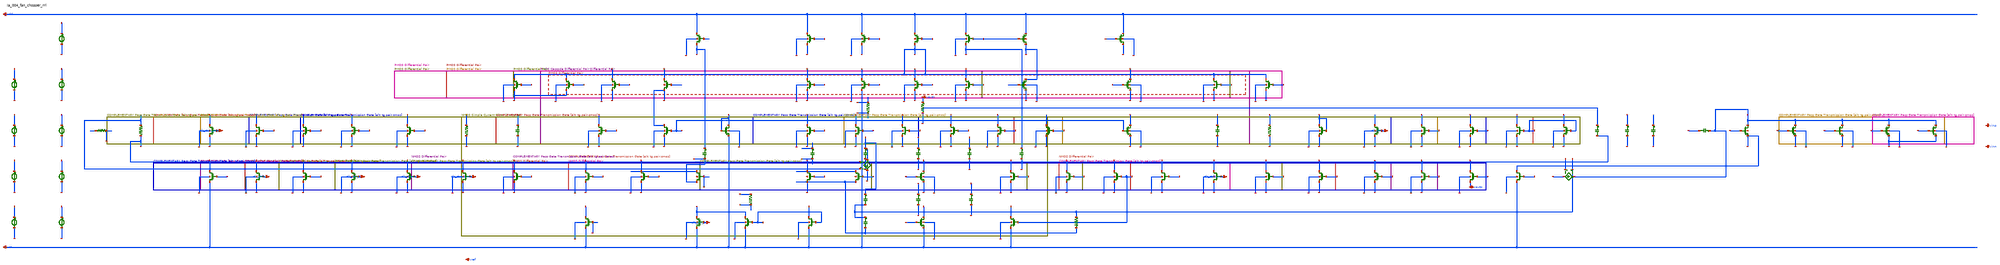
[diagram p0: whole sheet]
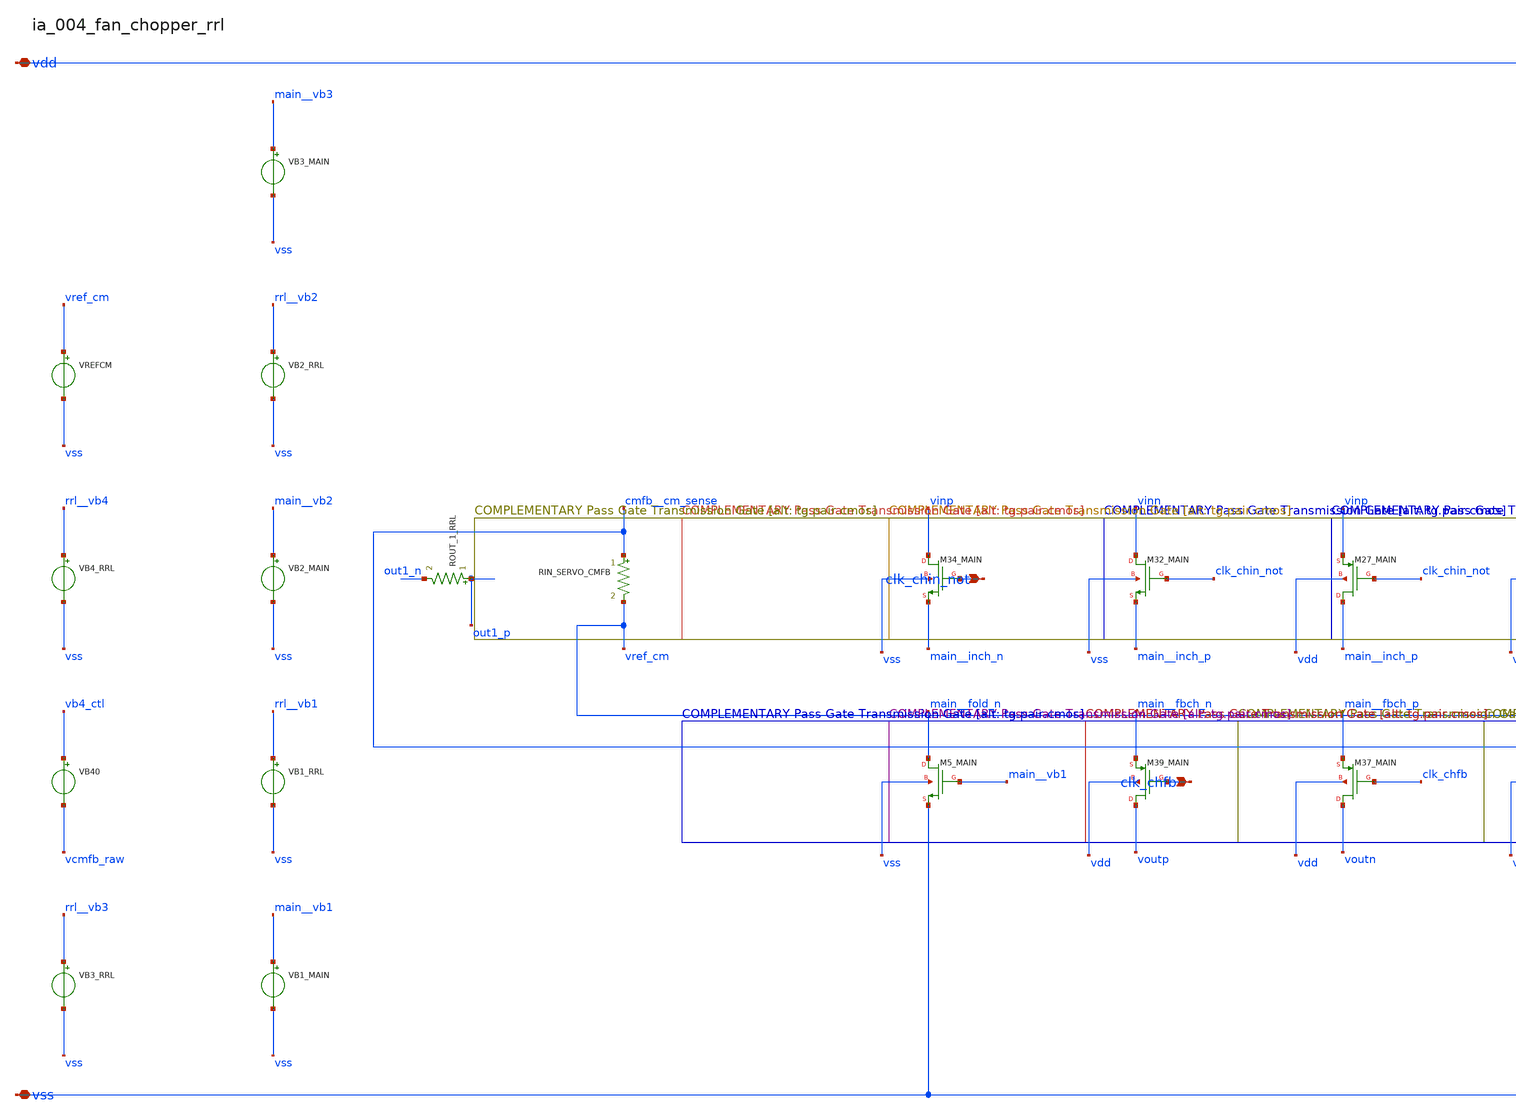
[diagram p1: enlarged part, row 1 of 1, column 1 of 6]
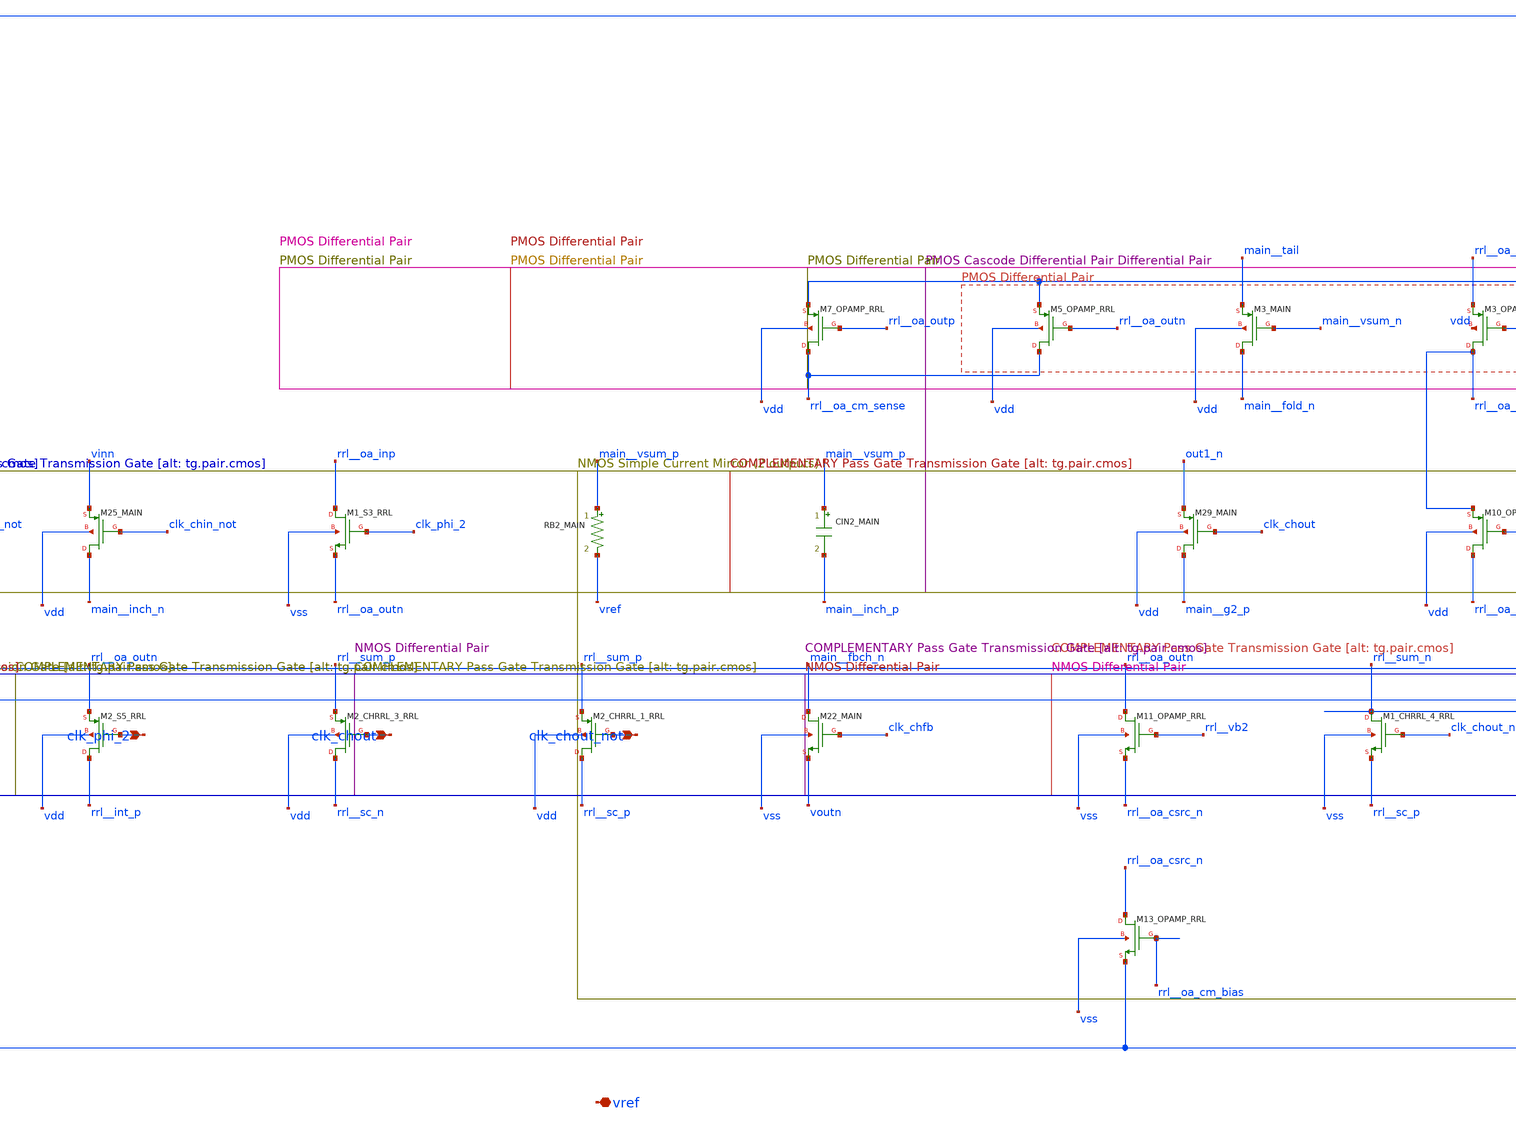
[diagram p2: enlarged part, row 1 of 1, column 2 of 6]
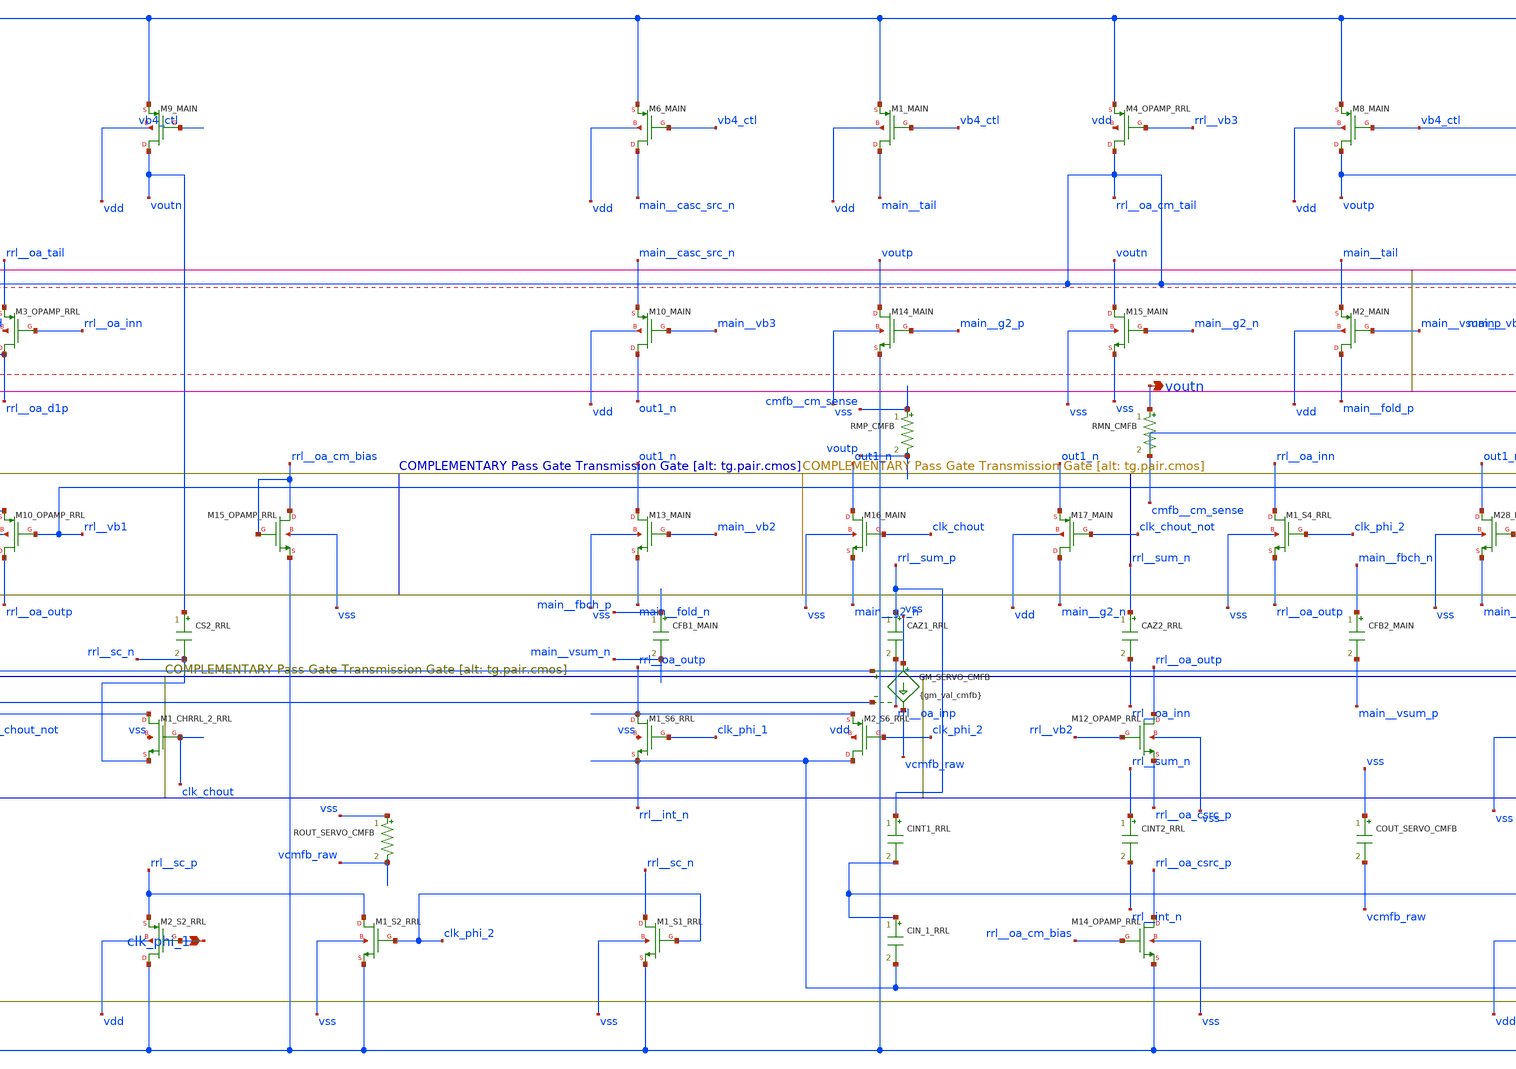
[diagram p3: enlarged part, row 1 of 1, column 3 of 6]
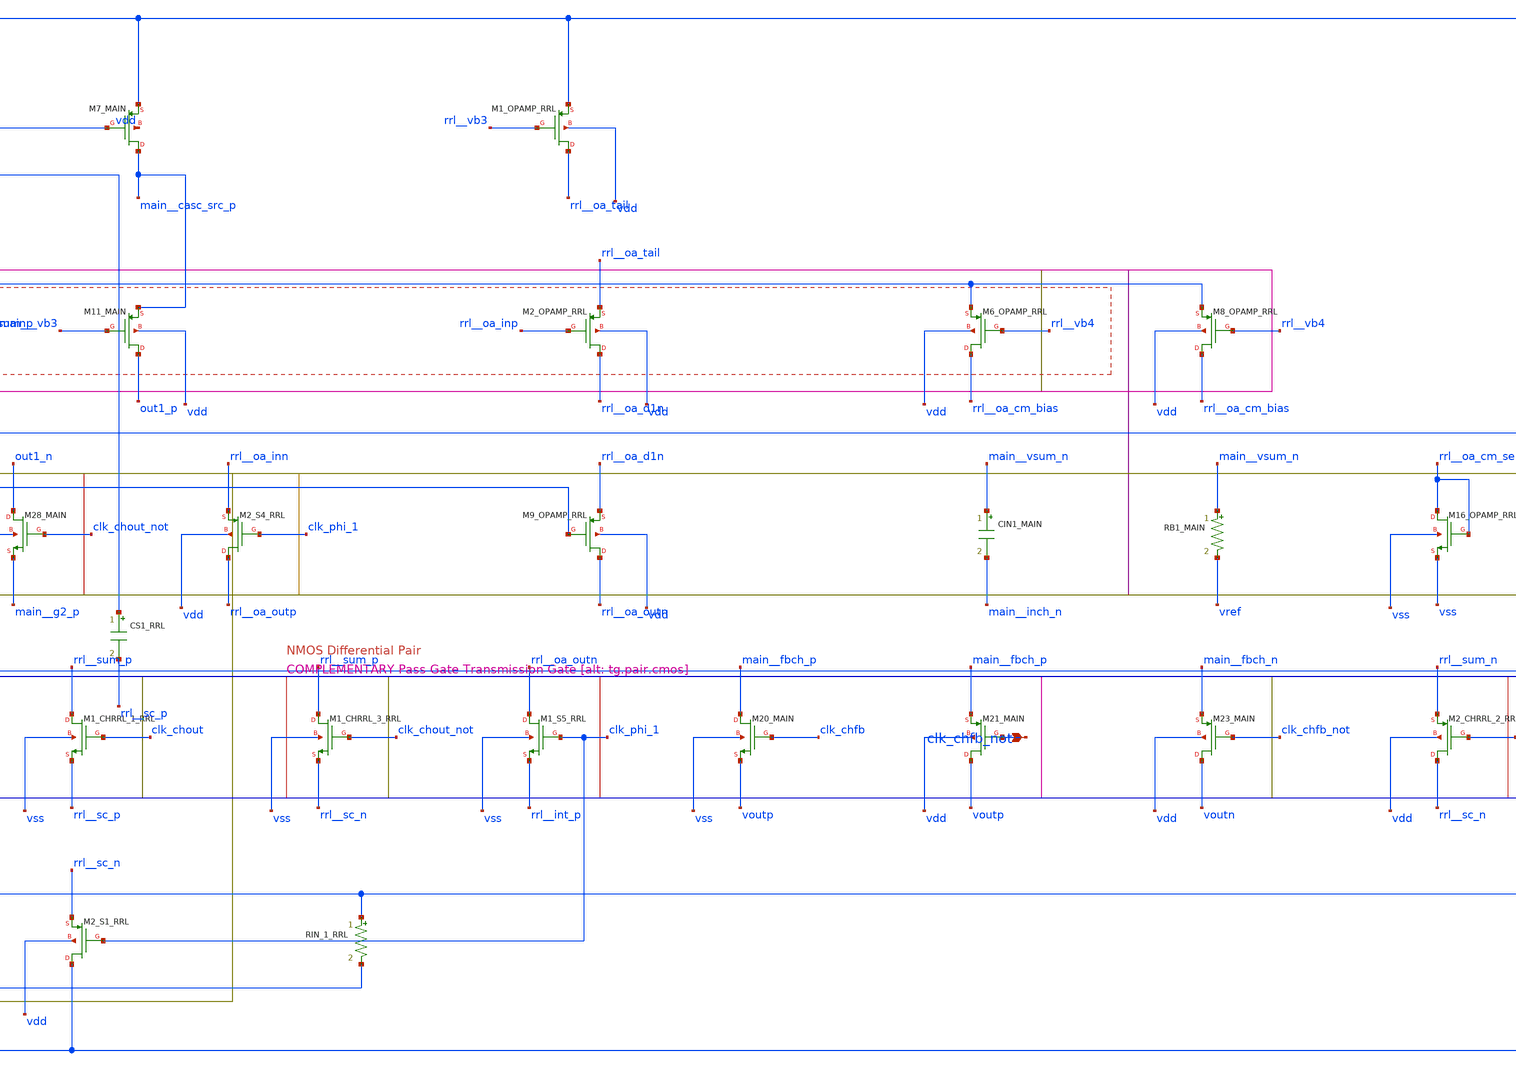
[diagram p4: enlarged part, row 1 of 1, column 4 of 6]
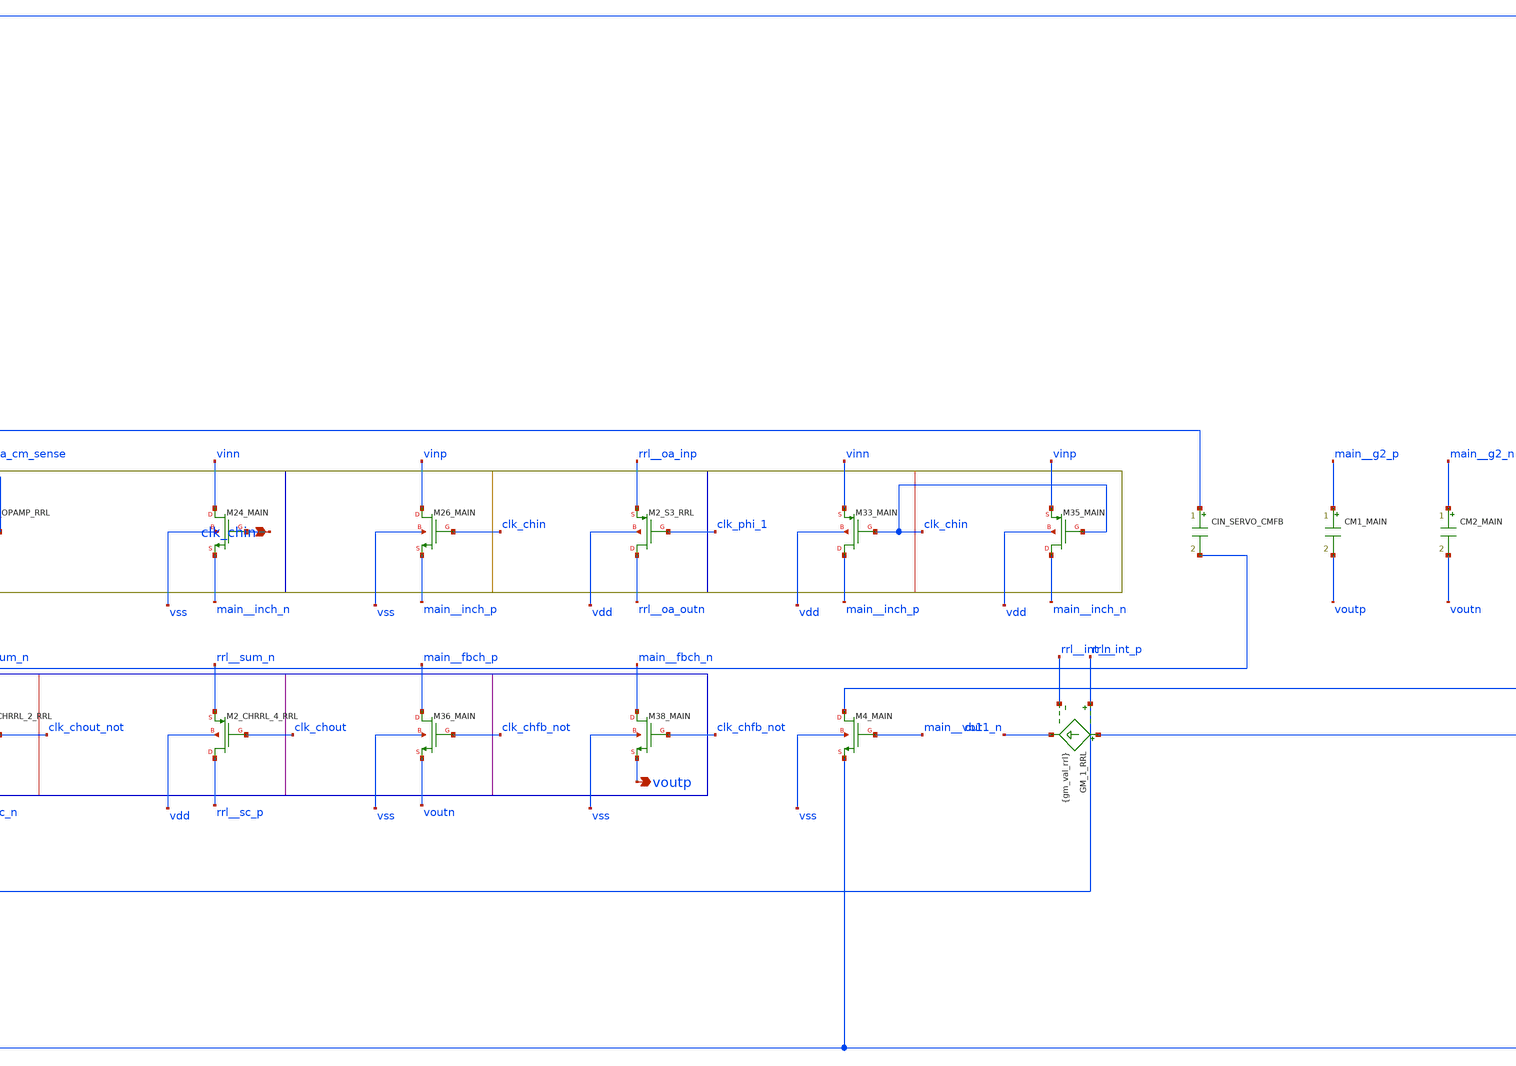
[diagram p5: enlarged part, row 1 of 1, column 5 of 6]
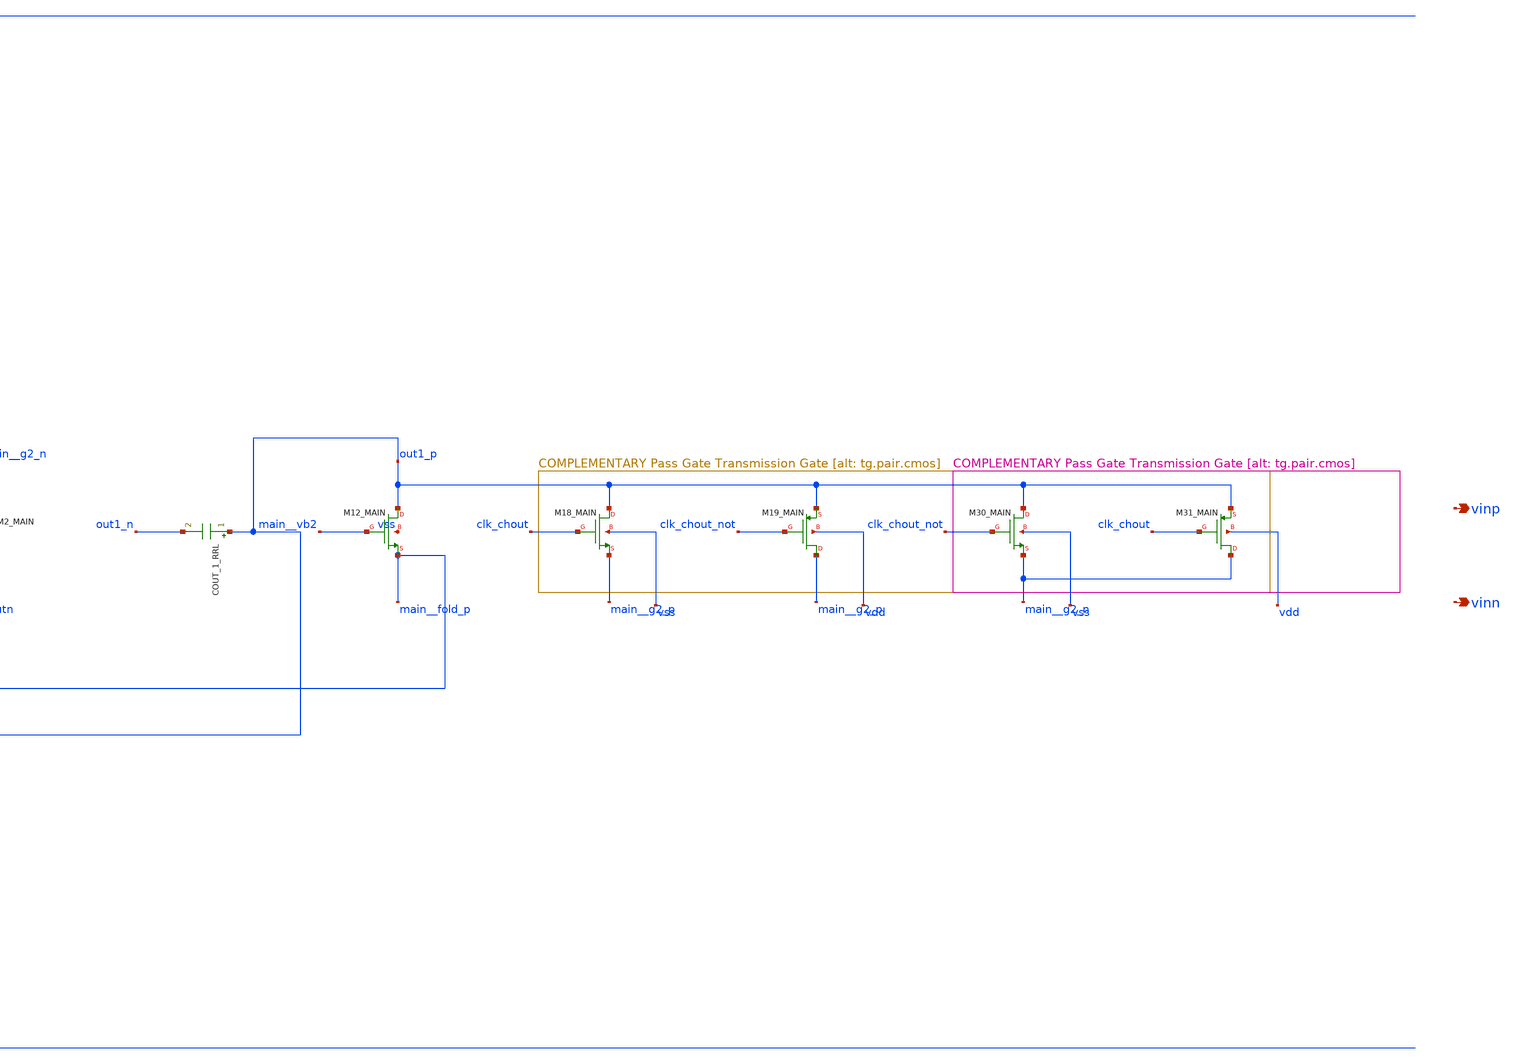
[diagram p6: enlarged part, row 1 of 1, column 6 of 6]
** sch_path: analog-db/raw/ia_004_fan_chopper_rrl/ia_004_fan_chopper_rrl_annotated.sch
**.subckt ia_004_fan_chopper_rrl_annotated clk_chin_not clk_phi_2 clk_chout clk_chout_not clk_phi_1
*+ clk_chin clk_chfb clk_chfb_not vdd vss voutn voutp vref vinp vinn
*.ipin clk_chin_not
*.ipin clk_phi_2
*.ipin clk_chout
*.ipin clk_chout_not
*.ipin clk_phi_1
*.ipin clk_chin
*.ipin clk_chfb
*.ipin clk_chfb_not
*.iopin vdd
*.iopin vss
*.opin voutn
*.opin voutp
*.iopin vref
*.opin vinp
*.opin vinn
CAZ1_RRL rrl__sum_p rrl__oa_inp 'x_dut_caz1_rrl_value' m=1
CAZ2_RRL rrl__sum_n rrl__oa_inn 'x_dut_caz2_rrl_value' m=1
CFB1_MAIN main__fbch_p main__vsum_n 'x_dut_cfb1_main_value' m=1
CFB2_MAIN main__fbch_n main__vsum_p 'x_dut_cfb2_main_value' m=1
CIN1_MAIN main__vsum_n main__inch_n 'x_dut_cin1_main_value' m=1
CIN2_MAIN main__vsum_p main__inch_p 'x_dut_cin2_main_value' m=1
CINT1_RRL rrl__sum_p rrl__int_p 'x_dut_cint1_rrl_value' m=1
CINT2_RRL rrl__sum_n rrl__int_n 'x_dut_cint2_rrl_value' m=1
CIN_1_RRL rrl__int_p rrl__int_n 'cin_val_rrl' m=1
CIN_SERVO_CMFB cmfb__cm_sense vref_cm 'cin_val_cmfb' m=1
CM1_MAIN main__g2_p voutp 'x_dut_cm1_main_value' m=1
CM2_MAIN main__g2_n voutn 'x_dut_cm2_main_value' m=1
COUT_1_RRL out1_p out1_n 'cout_val_rrl' m=1
COUT_SERVO_CMFB vss vcmfb_raw 'cout_val_cmfb' m=1
CS1_RRL voutp rrl__sc_p 'x_dut_cs1_rrl_value' m=1
CS2_RRL voutn rrl__sc_n 'x_dut_cs2_rrl_value' m=1
GM_1_RRL out1_p out1_n rrl__int_p rrl__int_n {gm_val_rrl}
GM_SERVO_CMFB vss vcmfb_raw vref_cm cmfb__cm_sense {gm_val_cmfb}
RB1_MAIN main__vsum_n vref 'x_dut_rb1_main_value' m=1
RB2_MAIN main__vsum_p vref 'x_dut_rb2_main_value' m=1
RIN_1_RRL rrl__int_p rrl__int_n 'rin_val_rrl' m=1
RIN_SERVO_CMFB cmfb__cm_sense vref_cm 'rin_val_cmfb' m=1
RMN_CMFB voutn cmfb__cm_sense 'x_dut_rmn_cmfb_value' m=1
RMP_CMFB cmfb__cm_sense voutp 'x_dut_rmp_cmfb_value' m=1
ROUT_1_RRL out1_p out1_n 'rout_val_rrl' m=1
ROUT_SERVO_CMFB vss vcmfb_raw 'rout_val_cmfb' m=1
VB1_MAIN main__vb1 vss dc {vb1_main}
VB1_RRL rrl__vb1 vss dc {vb1_rrl}
VB2_MAIN main__vb2 vss dc {vb2_main}
VB2_RRL rrl__vb2 vss dc {vb2_rrl}
VB3_MAIN main__vb3 vss dc {vb3_main}
VB3_RRL rrl__vb3 vss dc {vb3_rrl}
VB40 vb4_ctl vcmfb_raw dc {vb40}
VB4_RRL rrl__vb4 vss dc {vb4_rrl}
VREFCM vref_cm vss dc {vcm_ref}
XM10_MAIN out1_n main__vb3 main__casc_src_n vdd sg13_lv_pmos w=x_dut_xm10_main_w l=x_dut_xm10_main_l
+ ng=1 m=x_dut_xm10_main_m
XM10_OPAMP_RRL rrl__oa_outp rrl__vb1 rrl__oa_d1p vdd sg13_lv_pmos w=x_dut_xm10_opamp_rrl_w
+ l=x_dut_xm10_opamp_rrl_l ng=1 m=x_dut_xm10_opamp_rrl_m
XM11_MAIN out1_p main__vb3 main__casc_src_p vdd sg13_lv_pmos w=x_dut_xm11_main_w l=x_dut_xm11_main_l
+ ng=1 m=x_dut_xm11_main_m
XM11_OPAMP_RRL rrl__oa_outn rrl__vb2 rrl__oa_csrc_n vss sg13_lv_nmos w=x_dut_xm11_opamp_rrl_w
+ l=x_dut_xm11_opamp_rrl_l ng=1 m=x_dut_xm11_opamp_rrl_m
XM12_MAIN out1_p main__vb2 main__fold_p vss sg13_lv_nmos w=x_dut_xm12_main_w l=x_dut_xm12_main_l
+ ng=1 m=x_dut_xm12_main_m
XM12_OPAMP_RRL rrl__oa_outp rrl__vb2 rrl__oa_csrc_p vss sg13_lv_nmos w=x_dut_xm12_opamp_rrl_w
+ l=x_dut_xm12_opamp_rrl_l ng=1 m=x_dut_xm12_opamp_rrl_m
XM13_MAIN out1_n main__vb2 main__fold_n vss sg13_lv_nmos w=x_dut_xm13_main_w l=x_dut_xm13_main_l
+ ng=1 m=x_dut_xm13_main_m
XM13_OPAMP_RRL rrl__oa_csrc_n rrl__oa_cm_bias vss vss sg13_lv_nmos w=x_dut_xm13_opamp_rrl_w
+ l=x_dut_xm13_opamp_rrl_l ng=1 m=x_dut_xm13_opamp_rrl_m
XM14_MAIN voutp main__g2_p vss vss sg13_lv_nmos w=x_dut_xm14_main_w l=x_dut_xm14_main_l ng=1
+ m=x_dut_xm14_main_m
XM14_OPAMP_RRL rrl__oa_csrc_p rrl__oa_cm_bias vss vss sg13_lv_nmos w=x_dut_xm14_opamp_rrl_w
+ l=x_dut_xm14_opamp_rrl_l ng=1 m=x_dut_xm14_opamp_rrl_m
XM15_MAIN voutn main__g2_n vss vss sg13_lv_nmos w=x_dut_xm15_main_w l=x_dut_xm15_main_l ng=1
+ m=x_dut_xm15_main_m
XM15_OPAMP_RRL rrl__oa_cm_bias rrl__oa_cm_bias vss vss sg13_lv_nmos w=x_dut_xm15_opamp_rrl_w
+ l=x_dut_xm15_opamp_rrl_l ng=1 m=x_dut_xm15_opamp_rrl_m
XM16_MAIN out1_n clk_chout main__g2_n vss sg13_lv_nmos w=x_dut_xm16_main_w l=x_dut_xm16_main_l ng=1
+ m=x_dut_xm16_main_m
XM16_OPAMP_RRL rrl__oa_cm_sense rrl__oa_cm_sense vss vss sg13_lv_nmos w=x_dut_xm16_opamp_rrl_w
+ l=x_dut_xm16_opamp_rrl_l ng=1 m=x_dut_xm16_opamp_rrl_m
XM17_MAIN main__g2_n clk_chout_not out1_n vdd sg13_lv_pmos w=x_dut_xm17_main_w l=x_dut_xm17_main_l
+ ng=1 m=x_dut_xm17_main_m
XM18_MAIN out1_p clk_chout main__g2_p vss sg13_lv_nmos w=x_dut_xm18_main_w l=x_dut_xm18_main_l ng=1
+ m=x_dut_xm18_main_m
XM19_MAIN main__g2_p clk_chout_not out1_p vdd sg13_lv_pmos w=x_dut_xm19_main_w l=x_dut_xm19_main_l
+ ng=1 m=x_dut_xm19_main_m
XM1_CHRRL_1_RRL rrl__sum_p clk_chout rrl__sc_p vss sg13_lv_nmos w=x_dut_xm1_chrrl_1_rrl_w
+ l=x_dut_xm1_chrrl_1_rrl_l ng=1 m=x_dut_xm1_chrrl_1_rrl_m
XM1_CHRRL_2_RRL rrl__sum_n clk_chout rrl__sc_n vss sg13_lv_nmos w=x_dut_xm1_chrrl_2_rrl_w
+ l=x_dut_xm1_chrrl_2_rrl_l ng=1 m=x_dut_xm1_chrrl_2_rrl_m
XM1_CHRRL_3_RRL rrl__sum_p clk_chout_not rrl__sc_n vss sg13_lv_nmos w=x_dut_xm1_chrrl_3_rrl_w
+ l=x_dut_xm1_chrrl_3_rrl_l ng=1 m=x_dut_xm1_chrrl_3_rrl_m
XM1_CHRRL_4_RRL rrl__sum_n clk_chout_not rrl__sc_p vss sg13_lv_nmos w=x_dut_xm1_chrrl_4_rrl_w
+ l=x_dut_xm1_chrrl_4_rrl_l ng=1 m=x_dut_xm1_chrrl_4_rrl_m
XM1_MAIN main__tail vb4_ctl vdd vdd sg13_lv_pmos w=x_dut_xm1_main_w l=x_dut_xm1_main_l ng=1
+ m=x_dut_xm1_main_m
XM1_OPAMP_RRL rrl__oa_tail rrl__vb3 vdd vdd sg13_lv_pmos w=x_dut_xm1_opamp_rrl_w
+ l=x_dut_xm1_opamp_rrl_l ng=1 m=x_dut_xm1_opamp_rrl_m
XM1_S1_RRL rrl__sc_n clk_phi_2 vss vss sg13_lv_nmos w=x_dut_xm1_s1_rrl_w l=x_dut_xm1_s1_rrl_l ng=1
+ m=x_dut_xm1_s1_rrl_m
XM1_S2_RRL rrl__sc_p clk_phi_2 vss vss sg13_lv_nmos w=x_dut_xm1_s2_rrl_w l=x_dut_xm1_s2_rrl_l ng=1
+ m=x_dut_xm1_s2_rrl_m
XM1_S3_RRL rrl__oa_inp clk_phi_2 rrl__oa_outn vss sg13_lv_nmos w=x_dut_xm1_s3_rrl_w
+ l=x_dut_xm1_s3_rrl_l ng=1 m=x_dut_xm1_s3_rrl_m
XM1_S4_RRL rrl__oa_inn clk_phi_2 rrl__oa_outp vss sg13_lv_nmos w=x_dut_xm1_s4_rrl_w
+ l=x_dut_xm1_s4_rrl_l ng=1 m=x_dut_xm1_s4_rrl_m
XM1_S5_RRL rrl__oa_outn clk_phi_1 rrl__int_p vss sg13_lv_nmos w=x_dut_xm1_s5_rrl_w
+ l=x_dut_xm1_s5_rrl_l ng=1 m=x_dut_xm1_s5_rrl_m
XM1_S6_RRL rrl__oa_outp clk_phi_1 rrl__int_n vss sg13_lv_nmos w=x_dut_xm1_s6_rrl_w
+ l=x_dut_xm1_s6_rrl_l ng=1 m=x_dut_xm1_s6_rrl_m
XM20_MAIN main__fbch_p clk_chfb voutp vss sg13_lv_nmos w=x_dut_xm20_main_w l=x_dut_xm20_main_l ng=1
+ m=x_dut_xm20_main_m
XM21_MAIN voutp clk_chfb_not main__fbch_p vdd sg13_lv_pmos w=x_dut_xm21_main_w l=x_dut_xm21_main_l
+ ng=1 m=x_dut_xm21_main_m
XM22_MAIN main__fbch_n clk_chfb voutn vss sg13_lv_nmos w=x_dut_xm22_main_w l=x_dut_xm22_main_l ng=1
+ m=x_dut_xm22_main_m
XM23_MAIN voutn clk_chfb_not main__fbch_n vdd sg13_lv_pmos w=x_dut_xm23_main_w l=x_dut_xm23_main_l
+ ng=1 m=x_dut_xm23_main_m
XM24_MAIN vinn clk_chin main__inch_n vss sg13_lv_nmos w=x_dut_xm24_main_w l=x_dut_xm24_main_l ng=1
+ m=x_dut_xm24_main_m
XM25_MAIN main__inch_n clk_chin_not vinn vdd sg13_lv_pmos w=x_dut_xm25_main_w l=x_dut_xm25_main_l
+ ng=1 m=x_dut_xm25_main_m
XM26_MAIN vinp clk_chin main__inch_p vss sg13_lv_nmos w=x_dut_xm26_main_w l=x_dut_xm26_main_l ng=1
+ m=x_dut_xm26_main_m
XM27_MAIN main__inch_p clk_chin_not vinp vdd sg13_lv_pmos w=x_dut_xm27_main_w l=x_dut_xm27_main_l
+ ng=1 m=x_dut_xm27_main_m
XM28_MAIN out1_n clk_chout_not main__g2_p vss sg13_lv_nmos w=x_dut_xm28_main_w l=x_dut_xm28_main_l
+ ng=1 m=x_dut_xm28_main_m
XM29_MAIN main__g2_p clk_chout out1_n vdd sg13_lv_pmos w=x_dut_xm29_main_w l=x_dut_xm29_main_l ng=1
+ m=x_dut_xm29_main_m
XM2_CHRRL_1_RRL rrl__sc_p clk_chout_not rrl__sum_p vdd sg13_lv_pmos w=x_dut_xm2_chrrl_1_rrl_w
+ l=x_dut_xm2_chrrl_1_rrl_l ng=1 m=x_dut_xm2_chrrl_1_rrl_m
XM2_CHRRL_2_RRL rrl__sc_n clk_chout_not rrl__sum_n vdd sg13_lv_pmos w=x_dut_xm2_chrrl_2_rrl_w
+ l=x_dut_xm2_chrrl_2_rrl_l ng=1 m=x_dut_xm2_chrrl_2_rrl_m
XM2_CHRRL_3_RRL rrl__sc_n clk_chout rrl__sum_p vdd sg13_lv_pmos w=x_dut_xm2_chrrl_3_rrl_w
+ l=x_dut_xm2_chrrl_3_rrl_l ng=1 m=x_dut_xm2_chrrl_3_rrl_m
XM2_CHRRL_4_RRL rrl__sc_p clk_chout rrl__sum_n vdd sg13_lv_pmos w=x_dut_xm2_chrrl_4_rrl_w
+ l=x_dut_xm2_chrrl_4_rrl_l ng=1 m=x_dut_xm2_chrrl_4_rrl_m
XM2_MAIN main__fold_p main__vsum_p main__tail vdd sg13_lv_pmos w=x_dut_xm2_main_w l=x_dut_xm2_main_l
+ ng=1 m=x_dut_xm2_main_m
XM2_OPAMP_RRL rrl__oa_d1n rrl__oa_inp rrl__oa_tail vdd sg13_lv_pmos w=x_dut_xm2_opamp_rrl_w
+ l=x_dut_xm2_opamp_rrl_l ng=1 m=x_dut_xm2_opamp_rrl_m
XM2_S1_RRL vss clk_phi_1 rrl__sc_n vdd sg13_lv_pmos w=x_dut_xm2_s1_rrl_w l=x_dut_xm2_s1_rrl_l ng=1
+ m=x_dut_xm2_s1_rrl_m
XM2_S2_RRL vss clk_phi_1 rrl__sc_p vdd sg13_lv_pmos w=x_dut_xm2_s2_rrl_w l=x_dut_xm2_s2_rrl_l ng=1
+ m=x_dut_xm2_s2_rrl_m
XM2_S3_RRL rrl__oa_outn clk_phi_1 rrl__oa_inp vdd sg13_lv_pmos w=x_dut_xm2_s3_rrl_w
+ l=x_dut_xm2_s3_rrl_l ng=1 m=x_dut_xm2_s3_rrl_m
XM2_S4_RRL rrl__oa_outp clk_phi_1 rrl__oa_inn vdd sg13_lv_pmos w=x_dut_xm2_s4_rrl_w
+ l=x_dut_xm2_s4_rrl_l ng=1 m=x_dut_xm2_s4_rrl_m
XM2_S5_RRL rrl__int_p clk_phi_2 rrl__oa_outn vdd sg13_lv_pmos w=x_dut_xm2_s5_rrl_w
+ l=x_dut_xm2_s5_rrl_l ng=1 m=x_dut_xm2_s5_rrl_m
XM2_S6_RRL rrl__int_n clk_phi_2 rrl__oa_outp vdd sg13_lv_pmos w=x_dut_xm2_s6_rrl_w
+ l=x_dut_xm2_s6_rrl_l ng=1 m=x_dut_xm2_s6_rrl_m
XM30_MAIN out1_p clk_chout_not main__g2_n vss sg13_lv_nmos w=x_dut_xm30_main_w l=x_dut_xm30_main_l
+ ng=1 m=x_dut_xm30_main_m
XM31_MAIN main__g2_n clk_chout out1_p vdd sg13_lv_pmos w=x_dut_xm31_main_w l=x_dut_xm31_main_l ng=1
+ m=x_dut_xm31_main_m
XM32_MAIN vinn clk_chin_not main__inch_p vss sg13_lv_nmos w=x_dut_xm32_main_w l=x_dut_xm32_main_l
+ ng=1 m=x_dut_xm32_main_m
XM33_MAIN main__inch_p clk_chin vinn vdd sg13_lv_pmos w=x_dut_xm33_main_w l=x_dut_xm33_main_l ng=1
+ m=x_dut_xm33_main_m
XM34_MAIN vinp clk_chin_not main__inch_n vss sg13_lv_nmos w=x_dut_xm34_main_w l=x_dut_xm34_main_l
+ ng=1 m=x_dut_xm34_main_m
XM35_MAIN main__inch_n clk_chin vinp vdd sg13_lv_pmos w=x_dut_xm35_main_w l=x_dut_xm35_main_l ng=1
+ m=x_dut_xm35_main_m
XM36_MAIN main__fbch_p clk_chfb_not voutn vss sg13_lv_nmos w=x_dut_xm36_main_w l=x_dut_xm36_main_l
+ ng=1 m=x_dut_xm36_main_m
XM37_MAIN voutn clk_chfb main__fbch_p vdd sg13_lv_pmos w=x_dut_xm37_main_w l=x_dut_xm37_main_l ng=1
+ m=x_dut_xm37_main_m
XM38_MAIN main__fbch_n clk_chfb_not voutp vss sg13_lv_nmos w=x_dut_xm38_main_w l=x_dut_xm38_main_l
+ ng=1 m=x_dut_xm38_main_m
XM39_MAIN voutp clk_chfb main__fbch_n vdd sg13_lv_pmos w=x_dut_xm39_main_w l=x_dut_xm39_main_l ng=1
+ m=x_dut_xm39_main_m
XM3_MAIN main__fold_n main__vsum_n main__tail vdd sg13_lv_pmos w=x_dut_xm3_main_w l=x_dut_xm3_main_l
+ ng=1 m=x_dut_xm3_main_m
XM3_OPAMP_RRL rrl__oa_d1p rrl__oa_inn rrl__oa_tail vdd sg13_lv_pmos w=x_dut_xm3_opamp_rrl_w
+ l=x_dut_xm3_opamp_rrl_l ng=1 m=x_dut_xm3_opamp_rrl_m
XM4_MAIN main__fold_p main__vb1 vss vss sg13_lv_nmos w=x_dut_xm4_main_w l=x_dut_xm4_main_l ng=1
+ m=x_dut_xm4_main_m
XM4_OPAMP_RRL rrl__oa_cm_tail rrl__vb3 vdd vdd sg13_lv_pmos w=x_dut_xm4_opamp_rrl_w
+ l=x_dut_xm4_opamp_rrl_l ng=1 m=x_dut_xm4_opamp_rrl_m
XM5_MAIN main__fold_n main__vb1 vss vss sg13_lv_nmos w=x_dut_xm5_main_w l=x_dut_xm5_main_l ng=1
+ m=x_dut_xm5_main_m
XM5_OPAMP_RRL rrl__oa_cm_sense rrl__oa_outn rrl__oa_cm_tail vdd sg13_lv_pmos w=x_dut_xm5_opamp_rrl_w
+ l=x_dut_xm5_opamp_rrl_l ng=1 m=x_dut_xm5_opamp_rrl_m
XM6_MAIN main__casc_src_n vb4_ctl vdd vdd sg13_lv_pmos w=x_dut_xm6_main_w l=x_dut_xm6_main_l ng=1
+ m=x_dut_xm6_main_m
XM6_OPAMP_RRL rrl__oa_cm_bias rrl__vb4 rrl__oa_cm_tail vdd sg13_lv_pmos w=x_dut_xm6_opamp_rrl_w
+ l=x_dut_xm6_opamp_rrl_l ng=1 m=x_dut_xm6_opamp_rrl_m
XM7_MAIN main__casc_src_p vb4_ctl vdd vdd sg13_lv_pmos w=x_dut_xm7_main_w l=x_dut_xm7_main_l ng=1
+ m=x_dut_xm7_main_m
XM7_OPAMP_RRL rrl__oa_cm_sense rrl__oa_outp rrl__oa_cm_tail vdd sg13_lv_pmos w=x_dut_xm7_opamp_rrl_w
+ l=x_dut_xm7_opamp_rrl_l ng=1 m=x_dut_xm7_opamp_rrl_m
XM8_MAIN voutp vb4_ctl vdd vdd sg13_lv_pmos w=x_dut_xm8_main_w l=x_dut_xm8_main_l ng=1
+ m=x_dut_xm8_main_m
XM8_OPAMP_RRL rrl__oa_cm_bias rrl__vb4 rrl__oa_cm_tail vdd sg13_lv_pmos w=x_dut_xm8_opamp_rrl_w
+ l=x_dut_xm8_opamp_rrl_l ng=1 m=x_dut_xm8_opamp_rrl_m
XM9_MAIN voutn vb4_ctl vdd vdd sg13_lv_pmos w=x_dut_xm9_main_w l=x_dut_xm9_main_l ng=1
+ m=x_dut_xm9_main_m
XM9_OPAMP_RRL rrl__oa_outn rrl__vb1 rrl__oa_d1n vdd sg13_lv_pmos w=x_dut_xm9_opamp_rrl_w
+ l=x_dut_xm9_opamp_rrl_l ng=1 m=x_dut_xm9_opamp_rrl_m
**.ends
.end
